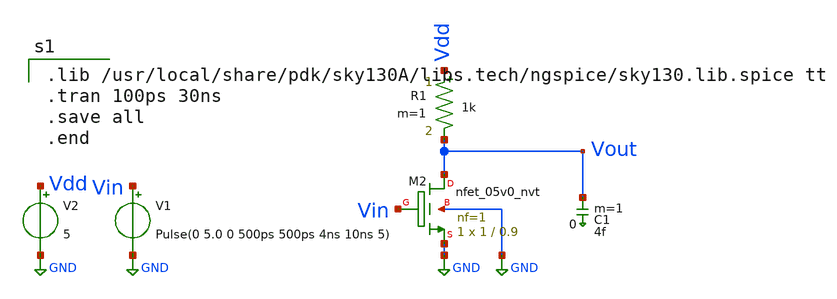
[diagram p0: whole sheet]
** sch_path: xschem/NMOS_inv.sch
**.subckt NMOS_inv
XM2 Vout Vin GND GND sky130_fd_pr__nfet_05v0_nvt L=0.9 W=1 nf=1 ad='int((1 + 1)/2) * 1 / 1 * 0.29' as='int((1 + 2)/2) * 1 / 1 * 0.29'
+ pd='2*int((1 + 1)/2) * (1 / 1 + 0.29)' ps='2*int((1 + 2)/2) * (1 / 1 + 0.29)' nrd='0.29 / 1 ' nrs='0.29 / 1 '
+ sa=0 sb=0 sd=0 mult=1 m=1
R1 Vdd Vout 1k m=1
C1 Vout 0 4f m=1
V1 Vin GND Pulse(0 5.0 0 500ps 500ps 4ns 10ns 5)
V2 Vdd GND 5
**** begin user architecture code

.lib /usr/local/share/pdk/sky130A/libs.tech/ngspice/sky130.lib.spice tt
.tran 100ps 30ns
.save all
.end

**** end user architecture code
**.ends
.GLOBAL GND
.end
